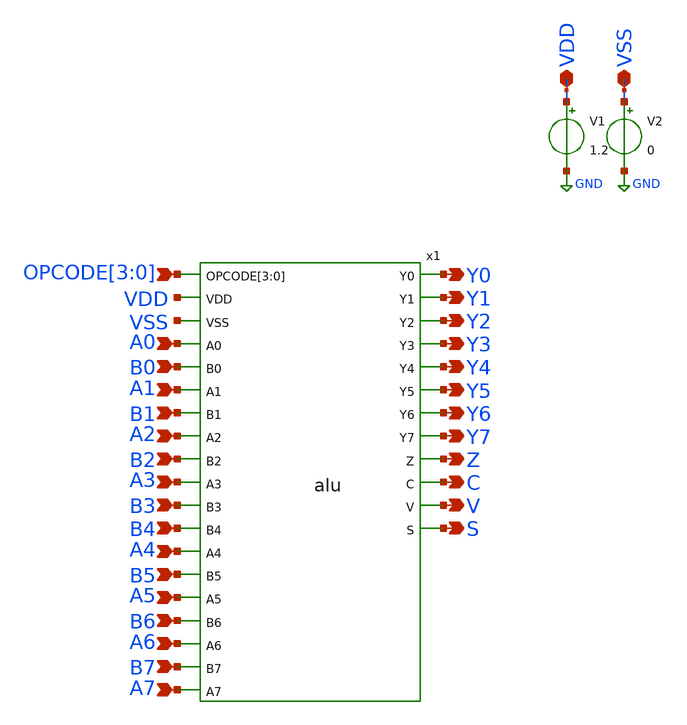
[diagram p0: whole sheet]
** sch_path: design/xschem/TEST_BENCHES/ALU_TB_AND.sch
**.subckt ALU_TB_AND VDD VSS A7 A6 A5 A4 A3 A2 A1 A0 B1 B2 B3 B0 B6 B7 B5 B4 Y0 Y1 Y2 Y3 Y4 Y5 Y6 Y7
*+ Z C V S OPCODE[3],OPCODE[2],OPCODE[1],OPCODE[0]
*.iopin VDD
*.iopin VSS
*.ipin A7
*.ipin A6
*.ipin A5
*.ipin A4
*.ipin A3
*.ipin A2
*.ipin A1
*.ipin A0
*.ipin B1
*.ipin B2
*.ipin B3
*.ipin B0
*.ipin B6
*.ipin B7
*.ipin B5
*.ipin B4
*.opin Y0
*.opin Y1
*.opin Y2
*.opin Y3
*.opin Y4
*.opin Y5
*.opin Y6
*.opin Y7
*.opin Z
*.opin C
*.opin V
*.opin S
*.ipin OPCODE[3],OPCODE[2],OPCODE[1],OPCODE[0]
V1 VDD GND 1.2
x1 OPCODE[3] OPCODE[2] OPCODE[1] OPCODE[0] A0 B0 Y0 Z VDD VSS A1 C B1 Y1 A2 V B2 Y2 S A3 Y3 B3 B4 Y4
+ A4 B5 A5 Y5 B6 Y6 A6 B7 Y7 A7 VSS VDD alu
V2 VSS GND 0
**** begin user architecture code

** opencircuitdesign pdks install
.lib $::SKYWATER_MODELS/sky130.lib.spice tt_mm




* SPICE Input for A, B, and OPCODE signals with custom sequences

* SPICE Input for A, B, and OPCODE signals with custom sequences

* Parameters
.param period = 4e-08
.param voltage = 1.2
.param end_time = 4e-07
.param tr = 1e-12
.param tf = 1e-12

V_A0 A0 0 PWL(0 0 1e-12 1.2 3.9999e-08 1.2 4e-08 0 4.0001e-08 0 7.9999e-08 0 8e-08 0 8.0001e-08 1.2
+ 1.19999e-07 1.2 1.2e-07 0 1.20001e-07 0 1.5999899999999998e-07 0 1.5999999999999998e-07 0
+ 1.6000099999999998e-07 1.2 1.9999899999999996e-07 1.2 1.9999999999999996e-07 0 2.0000099999999997e-07 0
+ 2.3999899999999995e-07 0 2.399999999999999e-07 0 2.400009999999999e-07 1.2 2.799989999999999e-07 1.2
+ 2.7999999999999986e-07 0 2.8000099999999983e-07 0 3.199989999999998e-07 0 3.199999999999998e-07 0 3.2000099999999977e-07
+ 1.2 3.5999899999999975e-07 1.2 3.5999999999999973e-07 0 3.600009999999997e-07 0 3.999989999999997e-07 0
+ 3.9999999999999966e-07 0)
V_A1 A1 0 PWL(0 0 1e-12 0 3.9999e-08 0 4e-08 0 4.0001e-08 0 7.9999e-08 0 8e-08 0 8.0001e-08 0
+ 1.19999e-07 0 1.2e-07 0 1.20001e-07 0 1.5999899999999998e-07 0 1.5999999999999998e-07 0 1.6000099999999998e-07
+ 0 1.9999899999999996e-07 0 1.9999999999999996e-07 0 2.0000099999999997e-07 0 2.3999899999999995e-07 0
+ 2.399999999999999e-07 0 2.400009999999999e-07 0 2.799989999999999e-07 0 2.7999999999999986e-07 0 2.8000099999999983e-07 0
+ 3.199989999999998e-07 0 3.199999999999998e-07 0 3.2000099999999977e-07 0 3.5999899999999975e-07 0 3.5999999999999973e-07
+ 0 3.600009999999997e-07 0 3.999989999999997e-07 0 3.9999999999999966e-07 0 4.0000099999999964e-07 0
+ 4.399989999999996e-07 0 4.399999999999996e-07 0)
V_A2 A2 0 PWL(0 0 1e-12 0 3.9999e-08 0 4e-08 0 4.0001e-08 0 7.9999e-08 0 8e-08 0 8.0001e-08 0
+ 1.19999e-07 0 1.2e-07 0 1.20001e-07 0 1.5999899999999998e-07 0 1.5999999999999998e-07 0 1.6000099999999998e-07
+ 0 1.9999899999999996e-07 0 1.9999999999999996e-07 0 2.0000099999999997e-07 0 2.3999899999999995e-07 0
+ 2.399999999999999e-07 0 2.400009999999999e-07 0 2.799989999999999e-07 0 2.7999999999999986e-07 0 2.8000099999999983e-07 0
+ 3.199989999999998e-07 0 3.199999999999998e-07 0 3.2000099999999977e-07 0 3.5999899999999975e-07 0 3.5999999999999973e-07
+ 0 3.600009999999997e-07 0 3.999989999999997e-07 0 3.9999999999999966e-07 0 4.0000099999999964e-07 0
+ 4.399989999999996e-07 0 4.399999999999996e-07 0)
V_A3 A3 0 PWL(0 0 1e-12 0 3.9999e-08 0 4e-08 0 4.0001e-08 0 7.9999e-08 0 8e-08 0 8.0001e-08 0
+ 1.19999e-07 0 1.2e-07 0 1.20001e-07 0 1.5999899999999998e-07 0 1.5999999999999998e-07 0 1.6000099999999998e-07
+ 0 1.9999899999999996e-07 0 1.9999999999999996e-07 0 2.0000099999999997e-07 0 2.3999899999999995e-07 0
+ 2.399999999999999e-07 0 2.400009999999999e-07 0 2.799989999999999e-07 0 2.7999999999999986e-07 0 2.8000099999999983e-07 0
+ 3.199989999999998e-07 0 3.199999999999998e-07 0 3.2000099999999977e-07 0 3.5999899999999975e-07 0 3.5999999999999973e-07
+ 0 3.600009999999997e-07 0 3.999989999999997e-07 0 3.9999999999999966e-07 0 4.0000099999999964e-07 0
+ 4.399989999999996e-07 0 4.399999999999996e-07 0)
V_A4 A4 0 PWL(0 0 1e-12 0 3.9999e-08 0 4e-08 0 4.0001e-08 0 7.9999e-08 0 8e-08 0 8.0001e-08 0
+ 1.19999e-07 0 1.2e-07 0 1.20001e-07 0 1.5999899999999998e-07 0 1.5999999999999998e-07 0 1.6000099999999998e-07
+ 0 1.9999899999999996e-07 0 1.9999999999999996e-07 0 2.0000099999999997e-07 0 2.3999899999999995e-07 0
+ 2.399999999999999e-07 0 2.400009999999999e-07 0 2.799989999999999e-07 0 2.7999999999999986e-07 0 2.8000099999999983e-07 0
+ 3.199989999999998e-07 0 3.199999999999998e-07 0 3.2000099999999977e-07 0 3.5999899999999975e-07 0 3.5999999999999973e-07
+ 0 3.600009999999997e-07 0 3.999989999999997e-07 0 3.9999999999999966e-07 0 4.0000099999999964e-07 0
+ 4.399989999999996e-07 0 4.399999999999996e-07 0)
V_A5 A5 0 PWL(0 0 1e-12 0 3.9999e-08 0 4e-08 0 4.0001e-08 0 7.9999e-08 0 8e-08 0 8.0001e-08 0
+ 1.19999e-07 0 1.2e-07 0 1.20001e-07 0 1.5999899999999998e-07 0 1.5999999999999998e-07 0 1.6000099999999998e-07
+ 0 1.9999899999999996e-07 0 1.9999999999999996e-07 0 2.0000099999999997e-07 0 2.3999899999999995e-07 0
+ 2.399999999999999e-07 0 2.400009999999999e-07 0 2.799989999999999e-07 0 2.7999999999999986e-07 0 2.8000099999999983e-07 0
+ 3.199989999999998e-07 0 3.199999999999998e-07 0 3.2000099999999977e-07 0 3.5999899999999975e-07 0 3.5999999999999973e-07
+ 0 3.600009999999997e-07 0 3.999989999999997e-07 0 3.9999999999999966e-07 0 4.0000099999999964e-07 0
+ 4.399989999999996e-07 0 4.399999999999996e-07 0)
V_A6 A6 0 PWL(0 0 1e-12 0 3.9999e-08 0 4e-08 0 4.0001e-08 0 7.9999e-08 0 8e-08 0 8.0001e-08 0
+ 1.19999e-07 0 1.2e-07 0 1.20001e-07 0 1.5999899999999998e-07 0 1.5999999999999998e-07 0 1.6000099999999998e-07
+ 0 1.9999899999999996e-07 0 1.9999999999999996e-07 0 2.0000099999999997e-07 0 2.3999899999999995e-07 0
+ 2.399999999999999e-07 0 2.400009999999999e-07 0 2.799989999999999e-07 0 2.7999999999999986e-07 0 2.8000099999999983e-07 0
+ 3.199989999999998e-07 0 3.199999999999998e-07 0 3.2000099999999977e-07 0 3.5999899999999975e-07 0 3.5999999999999973e-07
+ 0 3.600009999999997e-07 0 3.999989999999997e-07 0 3.9999999999999966e-07 0 4.0000099999999964e-07 0
+ 4.399989999999996e-07 0 4.399999999999996e-07 0)
V_A7 A7 0 PWL(0 0 1e-12 0 3.9999e-08 0 4e-08 0 4.0001e-08 0 7.9999e-08 0 8e-08 0 8.0001e-08 0
+ 1.19999e-07 0 1.2e-07 0 1.20001e-07 0 1.5999899999999998e-07 0 1.5999999999999998e-07 0 1.6000099999999998e-07
+ 0 1.9999899999999996e-07 0 1.9999999999999996e-07 0 2.0000099999999997e-07 0 2.3999899999999995e-07 0
+ 2.399999999999999e-07 0 2.400009999999999e-07 0 2.799989999999999e-07 0 2.7999999999999986e-07 0 2.8000099999999983e-07 0
+ 3.199989999999998e-07 0 3.199999999999998e-07 0 3.2000099999999977e-07 0 3.5999899999999975e-07 0 3.5999999999999973e-07
+ 0 3.600009999999997e-07 0 3.999989999999997e-07 0 3.9999999999999966e-07 0 4.0000099999999964e-07 0
+ 4.399989999999996e-07 0 4.399999999999996e-07 0)
V_B0 B0 0 PWL(0 0 1e-12 0 3.9999e-08 0 4e-08 0 4.0001e-08 0 7.9999e-08 0 8e-08 0 8.0001e-08 1.2
+ 1.19999e-07 1.2 1.2e-07 0 1.20001e-07 1.2 1.5999899999999998e-07 1.2 1.5999999999999998e-07 0
+ 1.6000099999999998e-07 0 1.9999899999999996e-07 0 1.9999999999999996e-07 0 2.0000099999999997e-07 0 2.3999899999999995e-07
+ 0 2.399999999999999e-07 0 2.400009999999999e-07 1.2 2.799989999999999e-07 1.2 2.7999999999999986e-07
+ 0 2.8000099999999983e-07 1.2 3.199989999999998e-07 1.2 3.199999999999998e-07 0 3.2000099999999977e-07
+ 0 3.5999899999999975e-07 0 3.5999999999999973e-07 0 3.600009999999997e-07 0 3.999989999999997e-07 0
+ 3.9999999999999966e-07 0)
V_B1 B1 0 PWL(0 0 1e-12 0 3.9999e-08 0 4e-08 0 4.0001e-08 0 7.9999e-08 0 8e-08 0 8.0001e-08 0
+ 1.19999e-07 0 1.2e-07 0 1.20001e-07 0 1.5999899999999998e-07 0 1.5999999999999998e-07 0 1.6000099999999998e-07
+ 0 1.9999899999999996e-07 0 1.9999999999999996e-07 0 2.0000099999999997e-07 0 2.3999899999999995e-07 0
+ 2.399999999999999e-07 0 2.400009999999999e-07 0 2.799989999999999e-07 0 2.7999999999999986e-07 0 2.8000099999999983e-07 0
+ 3.199989999999998e-07 0 3.199999999999998e-07 0 3.2000099999999977e-07 0 3.5999899999999975e-07 0 3.5999999999999973e-07
+ 0 3.600009999999997e-07 0 3.999989999999997e-07 0 3.9999999999999966e-07 0 4.0000099999999964e-07 0
+ 4.399989999999996e-07 0 4.399999999999996e-07 0)
V_B2 B2 0 PWL(0 0 1e-12 0 3.9999e-08 0 4e-08 0 4.0001e-08 0 7.9999e-08 0 8e-08 0 8.0001e-08 0
+ 1.19999e-07 0 1.2e-07 0 1.20001e-07 0 1.5999899999999998e-07 0 1.5999999999999998e-07 0 1.6000099999999998e-07
+ 0 1.9999899999999996e-07 0 1.9999999999999996e-07 0 2.0000099999999997e-07 0 2.3999899999999995e-07 0
+ 2.399999999999999e-07 0 2.400009999999999e-07 0 2.799989999999999e-07 0 2.7999999999999986e-07 0 2.8000099999999983e-07 0
+ 3.199989999999998e-07 0 3.199999999999998e-07 0 3.2000099999999977e-07 0 3.5999899999999975e-07 0 3.5999999999999973e-07
+ 0 3.600009999999997e-07 0 3.999989999999997e-07 0 3.9999999999999966e-07 0 4.0000099999999964e-07 0
+ 4.399989999999996e-07 0 4.399999999999996e-07 0)
V_B3 B3 0 PWL(0 0 1e-12 0 3.9999e-08 0 4e-08 0 4.0001e-08 0 7.9999e-08 0 8e-08 0 8.0001e-08 0
+ 1.19999e-07 0 1.2e-07 0 1.20001e-07 0 1.5999899999999998e-07 0 1.5999999999999998e-07 0 1.6000099999999998e-07
+ 0 1.9999899999999996e-07 0 1.9999999999999996e-07 0 2.0000099999999997e-07 0 2.3999899999999995e-07 0
+ 2.399999999999999e-07 0 2.400009999999999e-07 0 2.799989999999999e-07 0 2.7999999999999986e-07 0 2.8000099999999983e-07 0
+ 3.199989999999998e-07 0 3.199999999999998e-07 0 3.2000099999999977e-07 0 3.5999899999999975e-07 0 3.5999999999999973e-07
+ 0 3.600009999999997e-07 0 3.999989999999997e-07 0 3.9999999999999966e-07 0 4.0000099999999964e-07 0
+ 4.399989999999996e-07 0 4.399999999999996e-07 0)
V_B4 B4 0 PWL(0 0 1e-12 0 3.9999e-08 0 4e-08 0 4.0001e-08 0 7.9999e-08 0 8e-08 0 8.0001e-08 0
+ 1.19999e-07 0 1.2e-07 0 1.20001e-07 0 1.5999899999999998e-07 0 1.5999999999999998e-07 0 1.6000099999999998e-07
+ 0 1.9999899999999996e-07 0 1.9999999999999996e-07 0 2.0000099999999997e-07 0 2.3999899999999995e-07 0
+ 2.399999999999999e-07 0 2.400009999999999e-07 0 2.799989999999999e-07 0 2.7999999999999986e-07 0 2.8000099999999983e-07 0
+ 3.199989999999998e-07 0 3.199999999999998e-07 0 3.2000099999999977e-07 0 3.5999899999999975e-07 0 3.5999999999999973e-07
+ 0 3.600009999999997e-07 0 3.999989999999997e-07 0 3.9999999999999966e-07 0 4.0000099999999964e-07 0
+ 4.399989999999996e-07 0 4.399999999999996e-07 0)
V_B5 B5 0 PWL(0 0 1e-12 0 3.9999e-08 0 4e-08 0 4.0001e-08 0 7.9999e-08 0 8e-08 0 8.0001e-08 0
+ 1.19999e-07 0 1.2e-07 0 1.20001e-07 0 1.5999899999999998e-07 0 1.5999999999999998e-07 0 1.6000099999999998e-07
+ 0 1.9999899999999996e-07 0 1.9999999999999996e-07 0 2.0000099999999997e-07 0 2.3999899999999995e-07 0
+ 2.399999999999999e-07 0 2.400009999999999e-07 0 2.799989999999999e-07 0 2.7999999999999986e-07 0 2.8000099999999983e-07 0
+ 3.199989999999998e-07 0 3.199999999999998e-07 0 3.2000099999999977e-07 0 3.5999899999999975e-07 0 3.5999999999999973e-07
+ 0 3.600009999999997e-07 0 3.999989999999997e-07 0 3.9999999999999966e-07 0 4.0000099999999964e-07 0
+ 4.399989999999996e-07 0 4.399999999999996e-07 0)
V_B6 B6 0 PWL(0 0 1e-12 0 3.9999e-08 0 4e-08 0 4.0001e-08 0 7.9999e-08 0 8e-08 0 8.0001e-08 0
+ 1.19999e-07 0 1.2e-07 0 1.20001e-07 0 1.5999899999999998e-07 0 1.5999999999999998e-07 0 1.6000099999999998e-07
+ 0 1.9999899999999996e-07 0 1.9999999999999996e-07 0 2.0000099999999997e-07 0 2.3999899999999995e-07 0
+ 2.399999999999999e-07 0 2.400009999999999e-07 0 2.799989999999999e-07 0 2.7999999999999986e-07 0 2.8000099999999983e-07 0
+ 3.199989999999998e-07 0 3.199999999999998e-07 0 3.2000099999999977e-07 0 3.5999899999999975e-07 0 3.5999999999999973e-07
+ 0 3.600009999999997e-07 0 3.999989999999997e-07 0 3.9999999999999966e-07 0 4.0000099999999964e-07 0
+ 4.399989999999996e-07 0 4.399999999999996e-07 0)
V_B7 B7 0 PWL(0 0 1e-12 0 3.9999e-08 0 4e-08 0 4.0001e-08 0 7.9999e-08 0 8e-08 0 8.0001e-08 0
+ 1.19999e-07 0 1.2e-07 0 1.20001e-07 0 1.5999899999999998e-07 0 1.5999999999999998e-07 0 1.6000099999999998e-07
+ 0 1.9999899999999996e-07 0 1.9999999999999996e-07 0 2.0000099999999997e-07 0 2.3999899999999995e-07 0
+ 2.399999999999999e-07 0 2.400009999999999e-07 0 2.799989999999999e-07 0 2.7999999999999986e-07 0 2.8000099999999983e-07 0
+ 3.199989999999998e-07 0 3.199999999999998e-07 0 3.2000099999999977e-07 0 3.5999899999999975e-07 0 3.5999999999999973e-07
+ 0 3.600009999999997e-07 0 3.999989999999997e-07 0 3.9999999999999966e-07 0 4.0000099999999964e-07 0
+ 4.399989999999996e-07 0 4.399999999999996e-07 0)
V_OPCODE0 OPCODE[0] 0 PWL(0 0 1e-12 0 3.1999900000000003e-07 0 3.2e-07 0 3.20001e-07 0 6.39999e-07 0
+ 6.4e-07 0 6.40001e-07 0 9.59999e-07 0 9.600000000000001e-07 0 9.600010000000002e-07 0
+ 1.2799990000000002e-06 0 1.2800000000000002e-06 0 1.2800010000000003e-06 1.2 1.5999990000000003e-06 1.2
+ 1.6000000000000004e-06 0 1.6000010000000004e-06 1.2 1.9199990000000004e-06 1.2 1.9200000000000003e-06 0 1.920001e-06 1.2
+ 2.2399990000000003e-06 1.2 2.24e-06 0 2.240001e-06 1.2 2.559999e-06 1.2 2.5599999999999996e-06 0)
V_OPCODE1 OPCODE[1] 0 PWL(0 0 1e-12 0 3.1999900000000003e-07 0 3.2e-07 0 3.20001e-07 0 6.39999e-07 0
+ 6.4e-07 0 6.40001e-07 1.2 9.59999e-07 1.2 9.600000000000001e-07 0 9.600010000000002e-07 1.2
+ 1.2799990000000002e-06 1.2 1.2800000000000002e-06 0 1.2800010000000003e-06 0 1.5999990000000003e-06 0
+ 1.6000000000000004e-06 0 1.6000010000000004e-06 0 1.9199990000000004e-06 0 1.9200000000000003e-06 0 1.920001e-06 1.2
+ 2.2399990000000003e-06 1.2 2.24e-06 0 2.240001e-06 1.2 2.559999e-06 1.2 2.5599999999999996e-06 0)
V_OPCODE2 OPCODE[2] 0 PWL(0 0 1e-12 0 3.1999900000000003e-07 0 3.2e-07 0 3.20001e-07 1.2 6.39999e-07
+ 1.2 6.4e-07 0 6.40001e-07 0 9.59999e-07 0 9.600000000000001e-07 0 9.600010000000002e-07 1.2
+ 1.2799990000000002e-06 1.2 1.2800000000000002e-06 0 1.2800010000000003e-06 0 1.5999990000000003e-06 0
+ 1.6000000000000004e-06 0 1.6000010000000004e-06 1.2 1.9199990000000004e-06 1.2 1.9200000000000003e-06 0 1.920001e-06 0
+ 2.2399990000000003e-06 0 2.24e-06 0 2.240001e-06 1.2 2.559999e-06 1.2 2.5599999999999996e-06 0)
V_OPCODE3 OPCODE[3] 0 0
* Control block for transient simulation

.control
set color0=white
tran 1ns 400ns
set filetype ascii  ; This is the crucial line!
save V(Y0) V(Y1) V(Y2) V(Y3) V(Y4) V(Y5) V(Y6) V(Y7)
wrdata alu_tb.txt V(Y0) V(Y1) V(Y2) V(Y3) V(Y4) V(Y5) V(Y6) V(Y7) ; changed to .txt for clarity
plot V(Y0) V(Y1) V(Y2) V(Y3) V(Y4) V(Y5) V(Y6) V(Y7)
.endc



**** end user architecture code
**.ends
.GLOBAL GND
.end
